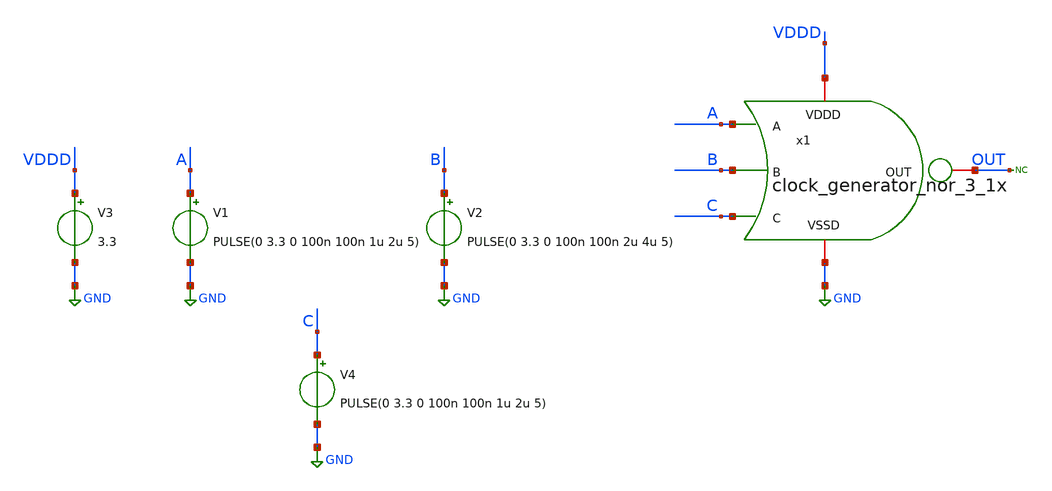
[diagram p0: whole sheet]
** sch_path: SAR_ADC/SAR_clock/xschem/clock_generator_nor_3_1x_tb.sch
**.subckt clock_generator_nor_3_1x_tb
x1 VDDD OUT GND A B C clock_generator_nor_3_1x
* noconn OUT
V1 A GND PULSE(0 3.3 0 100n 100n 1u 2u 5)
V3 VDDD GND 3.3
V2 B GND PULSE(0 3.3 0 100n 100n 2u 4u 5)
V4 C GND PULSE(0 3.3 0 100n 100n 1u 2u 5)
**** begin user architecture code



*Parameters
.options TEMPS= 27.0

*Models
.include /home/electrica/Documents/gf180_projects/pdk/gf180mcuC/libs.tech/ngspice/design.ngspice
.lib /home/electrica/Documents/gf180_projects/pdk/gf180mcuC/libs.tech/ngspice/sm141064.ngspice typical
.lib /home/electrica/Documents/gf180_projects/pdk/gf180mcuC/libs.tech/ngspice/smbb000149.ngspice typical


*Data to save
.save all

*Simulation
.control
tran 1n 30u
setplot dc1
plot V(C)+4 V(B)+8 V(A)+12 V(OUT)
set filetype=ascii
write clock_generator_nor_3_1x_tb_tran.raw

reset
unset filetype
op
save all
write clock_generator_nor_3_1x_tb.raw

.endc
.end



**** end user architecture code
**.ends

* expanding   symbol:
*+  /home/electrica/Documents/gf180_projects/gf180_work/PICO_contest/SAR_clock/clock_generator_nor_3_1x.sym # of pins=6
** sym_path: SAR_ADC/blocks/SAR_clock/clock_generator_nor_3_1x.sym
** sch_path: SAR_ADC/blocks/SAR_clock/clock_generator_nor_3_1x.sch
.subckt clock_generator_nor_3_1x VDDD OUT VSSD A B C
*.iopin VDDD
*.iopin VSSD
*.iopin OUT
*.ipin A
*.ipin B
*.ipin C
XM1 OUT B VSSD VSSD nfet_03v3 L=0.28u W=0.22u nf=1 ad='int((nf+1)/2) * W/nf * 0.18u' as='int((nf+2)/2) * W/nf * 0.18u'
+ pd='2*int((nf+1)/2) * (W/nf + 0.18u)' ps='2*int((nf+2)/2) * (W/nf + 0.18u)' nrd='0.18u / W' nrs='0.18u / W'
+ sa=0 sb=0 sd=0 m=1
XM2 OUT A VSSD VSSD nfet_03v3 L=0.28u W=0.22u nf=1 ad='int((nf+1)/2) * W/nf * 0.18u' as='int((nf+2)/2) * W/nf * 0.18u'
+ pd='2*int((nf+1)/2) * (W/nf + 0.18u)' ps='2*int((nf+2)/2) * (W/nf + 0.18u)' nrd='0.18u / W' nrs='0.18u / W'
+ sa=0 sb=0 sd=0 m=1
XM3 OUT C VSSD VSSD nfet_03v3 L=0.28u W=0.22u nf=1 ad='int((nf+1)/2) * W/nf * 0.18u' as='int((nf+2)/2) * W/nf * 0.18u'
+ pd='2*int((nf+1)/2) * (W/nf + 0.18u)' ps='2*int((nf+2)/2) * (W/nf + 0.18u)' nrd='0.18u / W' nrs='0.18u / W'
+ sa=0 sb=0 sd=0 m=1
XM4 OUT C net1 VDDD pfet_03v3 L=0.28u W=0.66u nf=1 ad='int((nf+1)/2) * W/nf * 0.18u' as='int((nf+2)/2) * W/nf * 0.18u'
+ pd='2*int((nf+1)/2) * (W/nf + 0.18u)' ps='2*int((nf+2)/2) * (W/nf + 0.18u)' nrd='0.18u / W' nrs='0.18u / W'
+ sa=0 sb=0 sd=0 m=1
XM5 net1 B net2 VDDD pfet_03v3 L=0.28u W=0.66u nf=1 ad='int((nf+1)/2) * W/nf * 0.18u' as='int((nf+2)/2) * W/nf * 0.18u'
+ pd='2*int((nf+1)/2) * (W/nf + 0.18u)' ps='2*int((nf+2)/2) * (W/nf + 0.18u)' nrd='0.18u / W' nrs='0.18u / W'
+ sa=0 sb=0 sd=0 m=1
XM6 net2 A VDDD VDDD pfet_03v3 L=0.28u W=0.66u nf=1 ad='int((nf+1)/2) * W/nf * 0.18u' as='int((nf+2)/2) * W/nf * 0.18u'
+ pd='2*int((nf+1)/2) * (W/nf + 0.18u)' ps='2*int((nf+2)/2) * (W/nf + 0.18u)' nrd='0.18u / W' nrs='0.18u / W'
+ sa=0 sb=0 sd=0 m=1
.ends

.GLOBAL GND
.end
